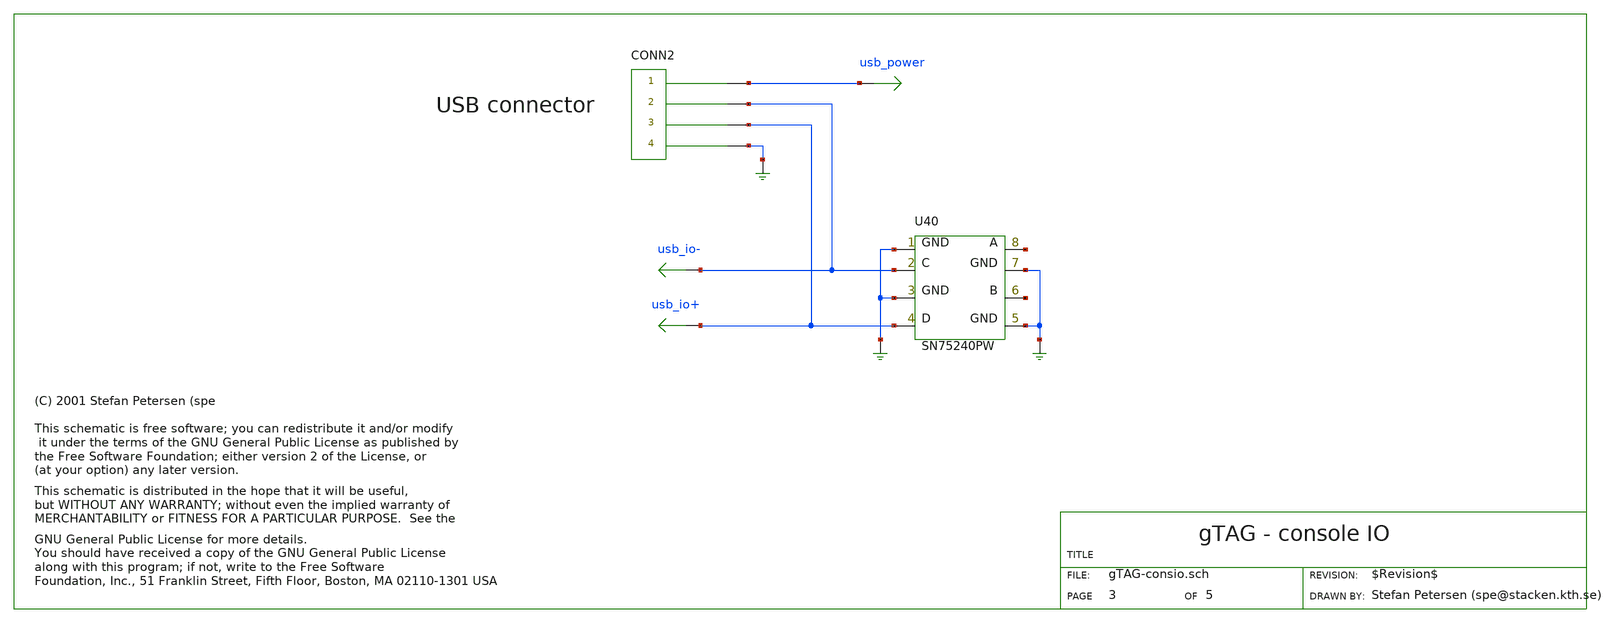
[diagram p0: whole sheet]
** sch_path: xschem-src/xschem_library/gschem_import/gTAG-consio.sch
* Copyright (C) 1998-2026 Stefan Frederik Schippers
* This program is free software; you can redistribute it and/or modify
* it under the terms of the GNU General Public License as published by
* the Free Software Foundation; either version 2 of the License, or
* (at your option) any later version.
* This program is distributed in the hope that it will be useful,
* but WITHOUT ANY WARRANTY; without even the implied warranty of
* MERCHANTABILITY or FITNESS FOR A PARTICULAR PURPOSE.  See the
* GNU General Public License for more details.
* You should have received a copy of the GNU General Public License
* along with this program; if not, write to the Free Software
* copyleft.sym
**.subckt gTAG-consio usb_io+ usb_io- usb_power
CONN2 usb_power usb_io- usb_io+ GND
U40 GND usb_io- GND usb_io+ GND net1 GND net2
**.ends
.end
